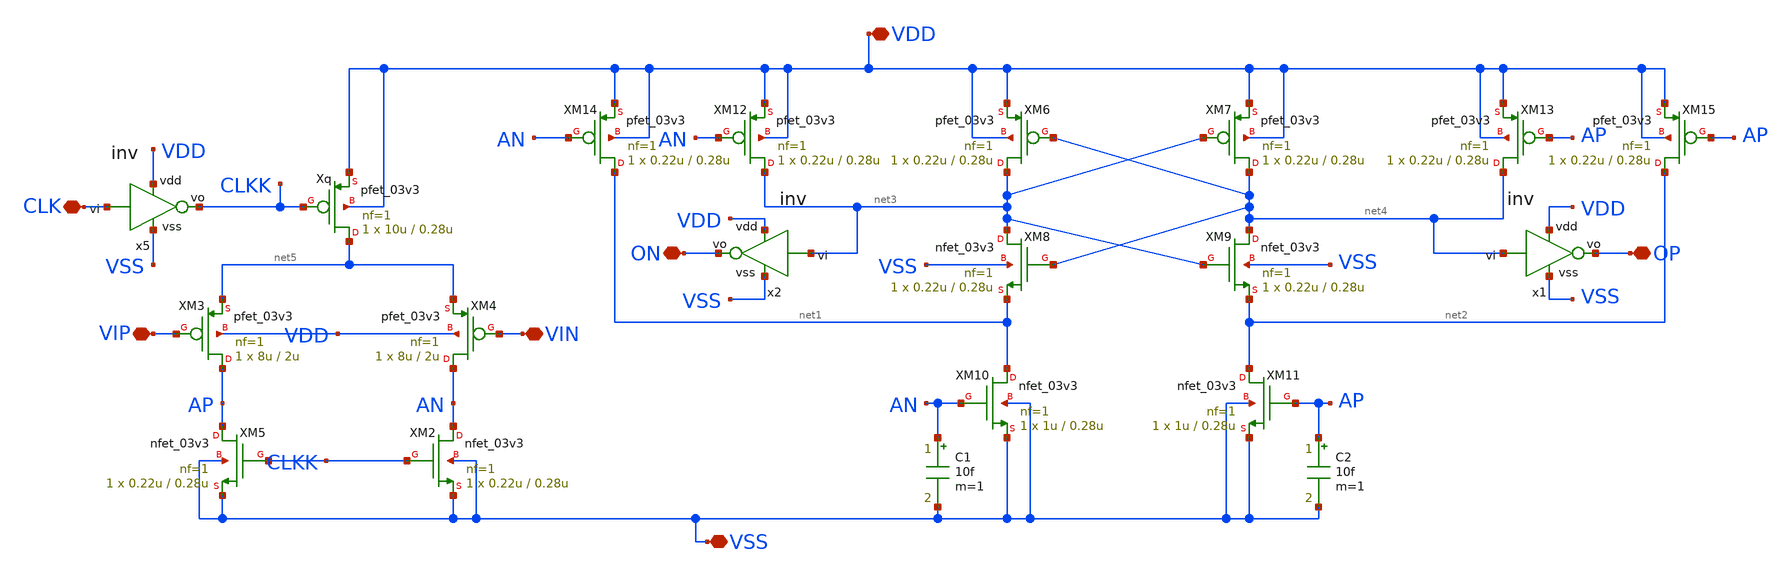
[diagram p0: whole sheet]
** sch_path: designs/sar_adc/comparator/StrongARM/strongARM.sch
**.subckt strongARM VSS VDD VIN VIP OP CLK ON
*.iopin VSS
*.iopin VDD
*.iopin VIN
*.iopin VIP
*.iopin OP
*.iopin CLK
*.iopin ON
Xq net5 CLKK VDD VDD pfet_03v3 L=0.28u W=10u nf=1 ad='int((nf+1)/2) * W/nf * 0.18u' as='int((nf+2)/2) * W/nf * 0.18u'
+ pd='2*int((nf+1)/2) * (W/nf + 0.18u)' ps='2*int((nf+2)/2) * (W/nf + 0.18u)' nrd='0.18u / W' nrs='0.18u / W'
+ sa=0 sb=0 sd=0 m=1
XM2 AN CLKK VSS VSS nfet_03v3 L=0.28u W=0.22u nf=1 ad='int((nf+1)/2) * W/nf * 0.18u' as='int((nf+2)/2) * W/nf * 0.18u'
+ pd='2*int((nf+1)/2) * (W/nf + 0.18u)' ps='2*int((nf+2)/2) * (W/nf + 0.18u)' nrd='0.18u / W' nrs='0.18u / W'
+ sa=0 sb=0 sd=0 m=1
XM3 AP VIP net5 VDD pfet_03v3 L=2u W=8u nf=1 ad='int((nf+1)/2) * W/nf * 0.18u' as='int((nf+2)/2) * W/nf * 0.18u'
+ pd='2*int((nf+1)/2) * (W/nf + 0.18u)' ps='2*int((nf+2)/2) * (W/nf + 0.18u)' nrd='0.18u / W' nrs='0.18u / W'
+ sa=0 sb=0 sd=0 m=1
XM4 AN VIN net5 VDD pfet_03v3 L=2u W=8u nf=1 ad='int((nf+1)/2) * W/nf * 0.18u' as='int((nf+2)/2) * W/nf * 0.18u'
+ pd='2*int((nf+1)/2) * (W/nf + 0.18u)' ps='2*int((nf+2)/2) * (W/nf + 0.18u)' nrd='0.18u / W' nrs='0.18u / W'
+ sa=0 sb=0 sd=0 m=1
XM5 AP CLKK VSS VSS nfet_03v3 L=0.28u W=0.22u nf=1 ad='int((nf+1)/2) * W/nf * 0.18u' as='int((nf+2)/2) * W/nf * 0.18u'
+ pd='2*int((nf+1)/2) * (W/nf + 0.18u)' ps='2*int((nf+2)/2) * (W/nf + 0.18u)' nrd='0.18u / W' nrs='0.18u / W'
+ sa=0 sb=0 sd=0 m=1
XM6 net3 net4 VDD VDD pfet_03v3 L=0.28u W=0.22u nf=1 ad='int((nf+1)/2) * W/nf * 0.18u' as='int((nf+2)/2) * W/nf * 0.18u'
+ pd='2*int((nf+1)/2) * (W/nf + 0.18u)' ps='2*int((nf+2)/2) * (W/nf + 0.18u)' nrd='0.18u / W' nrs='0.18u / W'
+ sa=0 sb=0 sd=0 m=1
XM7 net4 net3 VDD VDD pfet_03v3 L=0.28u W=0.22u nf=1 ad='int((nf+1)/2) * W/nf * 0.18u' as='int((nf+2)/2) * W/nf * 0.18u'
+ pd='2*int((nf+1)/2) * (W/nf + 0.18u)' ps='2*int((nf+2)/2) * (W/nf + 0.18u)' nrd='0.18u / W' nrs='0.18u / W'
+ sa=0 sb=0 sd=0 m=1
XM8 net3 net4 net1 VSS nfet_03v3 L=0.28u W=0.22u nf=1 ad='int((nf+1)/2) * W/nf * 0.18u' as='int((nf+2)/2) * W/nf * 0.18u'
+ pd='2*int((nf+1)/2) * (W/nf + 0.18u)' ps='2*int((nf+2)/2) * (W/nf + 0.18u)' nrd='0.18u / W' nrs='0.18u / W'
+ sa=0 sb=0 sd=0 m=1
XM9 net4 net3 net2 VSS nfet_03v3 L=0.28u W=0.22u nf=1 ad='int((nf+1)/2) * W/nf * 0.18u' as='int((nf+2)/2) * W/nf * 0.18u'
+ pd='2*int((nf+1)/2) * (W/nf + 0.18u)' ps='2*int((nf+2)/2) * (W/nf + 0.18u)' nrd='0.18u / W' nrs='0.18u / W'
+ sa=0 sb=0 sd=0 m=1
XM10 net1 AN VSS VSS nfet_03v3 L=0.28u W=1u nf=1 ad='int((nf+1)/2) * W/nf * 0.18u' as='int((nf+2)/2) * W/nf * 0.18u'
+ pd='2*int((nf+1)/2) * (W/nf + 0.18u)' ps='2*int((nf+2)/2) * (W/nf + 0.18u)' nrd='0.18u / W' nrs='0.18u / W'
+ sa=0 sb=0 sd=0 m=1
XM11 net2 AP VSS VSS nfet_03v3 L=0.28u W=1u nf=1 ad='int((nf+1)/2) * W/nf * 0.18u' as='int((nf+2)/2) * W/nf * 0.18u'
+ pd='2*int((nf+1)/2) * (W/nf + 0.18u)' ps='2*int((nf+2)/2) * (W/nf + 0.18u)' nrd='0.18u / W' nrs='0.18u / W'
+ sa=0 sb=0 sd=0 m=1
XM12 net3 AN VDD VDD pfet_03v3 L=0.28u W=0.22u nf=1 ad='int((nf+1)/2) * W/nf * 0.18u' as='int((nf+2)/2) * W/nf * 0.18u'
+ pd='2*int((nf+1)/2) * (W/nf + 0.18u)' ps='2*int((nf+2)/2) * (W/nf + 0.18u)' nrd='0.18u / W' nrs='0.18u / W'
+ sa=0 sb=0 sd=0 m=1
XM13 net4 AP VDD VDD pfet_03v3 L=0.28u W=0.22u nf=1 ad='int((nf+1)/2) * W/nf * 0.18u' as='int((nf+2)/2) * W/nf * 0.18u'
+ pd='2*int((nf+1)/2) * (W/nf + 0.18u)' ps='2*int((nf+2)/2) * (W/nf + 0.18u)' nrd='0.18u / W' nrs='0.18u / W'
+ sa=0 sb=0 sd=0 m=1
XM14 net1 AN VDD VDD pfet_03v3 L=0.28u W=0.22u nf=1 ad='int((nf+1)/2) * W/nf * 0.18u' as='int((nf+2)/2) * W/nf * 0.18u'
+ pd='2*int((nf+1)/2) * (W/nf + 0.18u)' ps='2*int((nf+2)/2) * (W/nf + 0.18u)' nrd='0.18u / W' nrs='0.18u / W'
+ sa=0 sb=0 sd=0 m=1
XM15 net2 AP VDD VDD pfet_03v3 L=0.28u W=0.22u nf=1 ad='int((nf+1)/2) * W/nf * 0.18u' as='int((nf+2)/2) * W/nf * 0.18u'
+ pd='2*int((nf+1)/2) * (W/nf + 0.18u)' ps='2*int((nf+2)/2) * (W/nf + 0.18u)' nrd='0.18u / W' nrs='0.18u / W'
+ sa=0 sb=0 sd=0 m=1
C1 AN VSS 10f m=1
C2 AP VSS 10f m=1
x1 VDD net4 OP VSS inv
x2 VDD net3 ON VSS inv
x5 VDD CLK CLKK VSS inv
**.ends
.end
